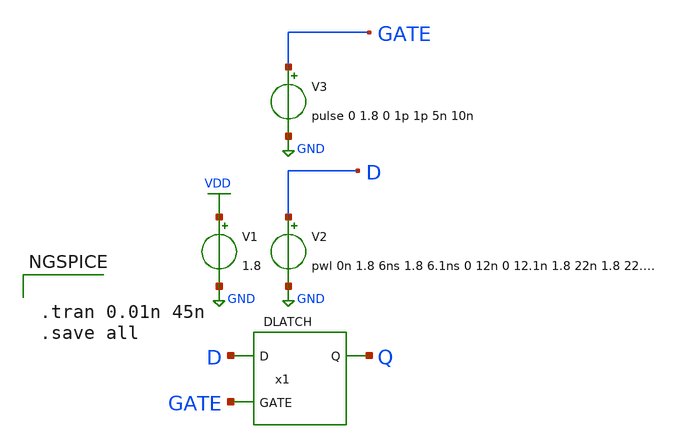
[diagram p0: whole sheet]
** sch_path: archives/lib/xschem/test_DLATCH.sch
**.subckt test_DLATCH
V2 D GND pwl 0n 1.8 6ns 1.8 6.1ns 0 12n 0 12.1n 1.8 22n 1.8 22.1n 0 27n 0 27.1n 1.8 34n 1.8 34.1n 0
V1 VDD GND 1.8
V3 GATE GND pulse 0 1.8 0 1p 1p 5n 10n
x1 GATE Q D VDD GND DLATCH
**** begin user architecture code

.lib $::SKYWATER_MODELS/sky130.lib.spice tt


**** end user architecture code
**.ends
.GLOBAL VDD
.GLOBAL GND
**** begin user architecture code


.tran 0.01n 45n
.save all


**** end user architecture code
.end
